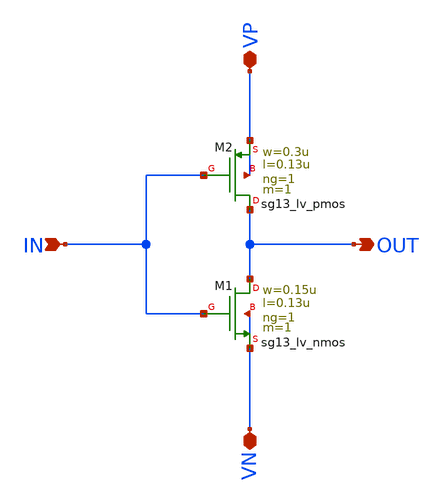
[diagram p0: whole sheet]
** sch_path: 30_MHz_Fractional_N_PLL/design_data/xschem/INV.sch
**.subckt INV VN VP IN OUT
*.iopin VN
*.iopin VP
*.ipin IN
*.opin OUT
XM1 OUT IN VN VN sg13_lv_nmos w=0.15u l=0.13u ng=1 m=1 mm_ok=1
XM2 OUT IN VP VP sg13_lv_pmos w=0.3u l=0.13u ng=1 m=1 mm_ok=1
**.ends
.end
